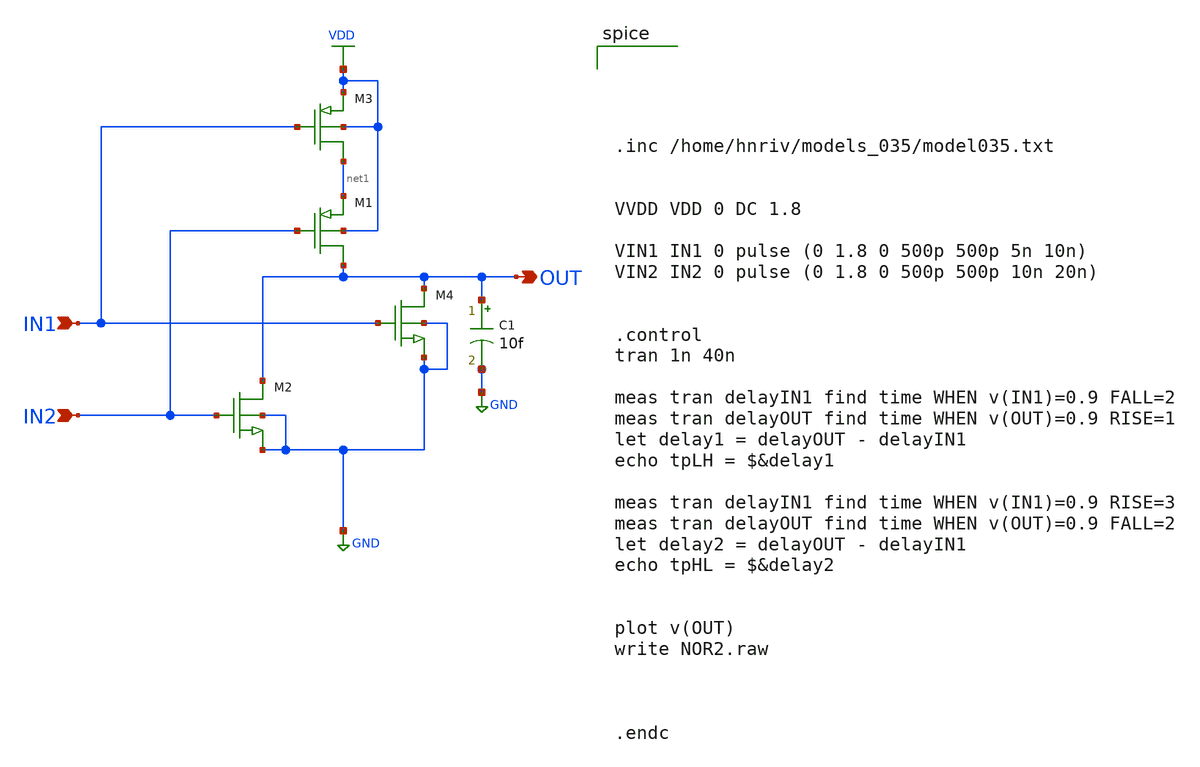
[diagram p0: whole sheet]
** sch_path: NOR2.sch
**.subckt NOR2 OUT IN1 IN2
*.opin OUT
*.ipin IN1
*.ipin IN2
M1 OUT IN2 net1 VDD pch w=3u l=0.35u as=0 ps=0 ad=0 pd=0 m=1
M2 OUT IN2 GND GND nch w=1u l=0.35u as=0 ps=0 ad=0 pd=0 m=1
M3 net1 IN1 VDD VDD pch w=3u l=0.35u as=0 ps=0 ad=0 pd=0 m=1
M4 OUT IN1 GND GND nch w=1u l=0.35u as=0 ps=0 ad=0 pd=0 m=1
C1 OUT GND 10f m=1
**** begin user architecture code





.inc /home/hnriv/models_035/model035.txt


VVDD VDD 0 DC 1.8

VIN1 IN1 0 pulse (0 1.8 0 500p 500p 5n 10n)
VIN2 IN2 0 pulse (0 1.8 0 500p 500p 10n 20n)


.control
tran 1n 40n

meas tran delayIN1 find time WHEN v(IN1)=0.9 FALL=2
meas tran delayOUT find time WHEN v(OUT)=0.9 RISE=1
let delay1 = delayOUT - delayIN1
echo tpLH = $&delay1

meas tran delayIN1 find time WHEN v(IN1)=0.9 RISE=3
meas tran delayOUT find time WHEN v(OUT)=0.9 FALL=2
let delay2 = delayOUT - delayIN1
echo tpHL = $&delay2


plot v(OUT)
write NOR2.raw



.endc

**** end user architecture code
**.ends
.GLOBAL VDD
.GLOBAL GND
.end
